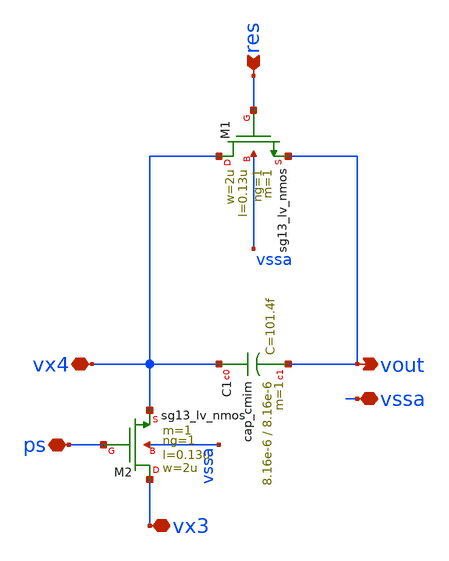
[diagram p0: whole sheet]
** sch_path: 5_Design/4_Layout/Team 5/splitUpSimulationsAndSchematics/integ_5_split5.sch
**.subckt integ_5_split5 res vssa vout vx3 ps vx4
*.ipin res
*.iopin vssa
*.opin vout
*.iopin vx3
*.iopin ps
*.iopin vx4
XM1 vx4 res vout vssa sg13_lv_nmos w=2u l=0.13u ng=1 m=1 mm_ok=1
XC1 vx4 vout cap_cmim w=8.16e-6 l=8.16e-6 m=1 mm_ok=1
XM2 vx3 ps vx4 vssa sg13_lv_nmos w=2u l=0.13u ng=1 m=1 mm_ok=1
**.ends
.end
